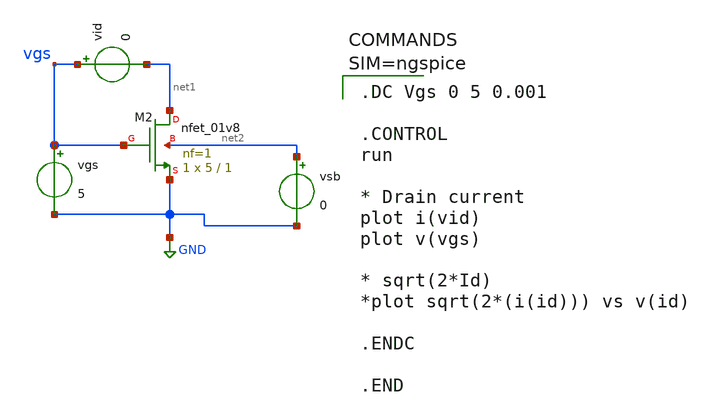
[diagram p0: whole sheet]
** sch_path: xschem/nmos.sch
**.subckt nmos
XM2 net1 vgs GND net2 sky130_fd_pr__nfet_01v8 L=1 W=5 nf=1 ad='int((1 + 1)/2) * 5 / 1 * 0.29' as='int((1 + 2)/2) * 5 / 1 * 0.29'
+ pd='2*int((1 + 1)/2) * (5 / 1 + 0.29)' ps='2*int((1 + 2)/2) * (5 / 1 + 0.29)' nrd='0.29 / 5 ' nrs='0.29 / 5 '
+ sa=0 sb=0 sd=0 mult=1 m=1
vgs vgs GND 5
vsb net2 GND 0
vid vgs net1 0
**** begin user architecture code


.DC Vgs 0 5 0.001

.CONTROL
run

* Drain current
plot i(vid)
plot v(vgs)

* sqrt(2*Id)
*plot sqrt(2*(i(id))) vs v(id)

.ENDC

.END




** opencircuitdesign pdks install
.lib $::SKYWATER_MODELS/sky130.lib.spice tt

**** end user architecture code
**.ends
.GLOBAL GND
.end
